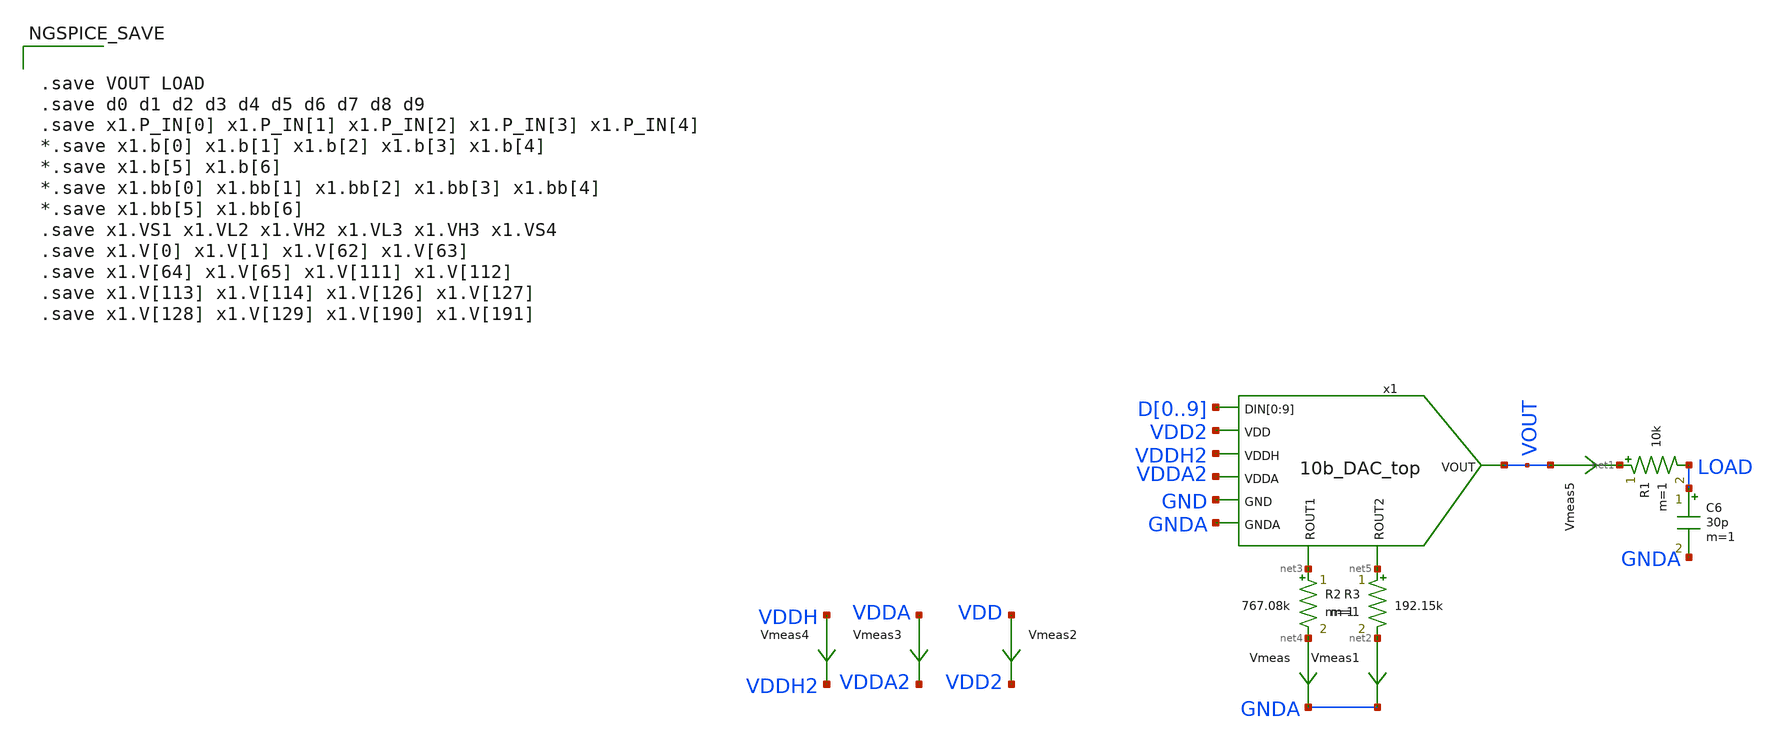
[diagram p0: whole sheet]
** sch_path: xschem/10b_DAC_noise-tb.sch
.lib $::SKYWATER_MODELS/sky130.lib.spice tt
.include $::SKYWATER_STDCELLS/sky130_fd_sc_hd.spice

**.subckt 10b_DAC_noise-tb
C6 LOAD GNDA 30p m=1
R1 net1 LOAD 10k m=1
Vmeas1 net2 GNDA 0
.save i(vmeas1)
R2 net3 net4 767.08k m=1
Vmeas net4 GNDA 0
.save i(vmeas)
R3 net5 net2 192.15k m=1
Vmeas2 VDD VDD2 0
.save i(vmeas2)
x1 D0 D1 D2 D3 D4 D5 D6 D7 D8 D9 VDD2 VDDH2 VDDA2 GND GNDA VOUT net3 net5 10b_DAC_top
Vmeas3 VDDA VDDA2 0
.save i(vmeas3)
Vmeas4 VDDH VDDH2 0
.save i(vmeas4)
Vmeas5 VOUT net1 0
.save i(vmeas5)
**** begin user architecture code


.save VOUT LOAD
.save d0 d1 d2 d3 d4 d5 d6 d7 d8 d9
.save x1.P_IN[0] x1.P_IN[1] x1.P_IN[2] x1.P_IN[3] x1.P_IN[4]
*.save x1.b[0] x1.b[1] x1.b[2] x1.b[3] x1.b[4]
*.save x1.b[5] x1.b[6]
*.save x1.bb[0] x1.bb[1] x1.bb[2] x1.bb[3] x1.bb[4]
*.save x1.bb[5] x1.bb[6]
.save x1.VS1 x1.VL2 x1.VH2 x1.VL3 x1.VH3 x1.VS4
.save x1.V[0] x1.V[1] x1.V[62] x1.V[63]
.save x1.V[64] x1.V[65] x1.V[111] x1.V[112]
.save x1.V[113] x1.V[114] x1.V[126] x1.V[127]
.save x1.V[128] x1.V[129] x1.V[190] x1.V[191]





  *.options wnflag=0 bypass=1
  .option wnflag=1
  .option safecurrents
  *.option klu
  .options solver=klu nomod
  .options method=gear rawfile=binary
  *.options reltol=1e-2 abstol=1e-12 chgtol=1e-14
  ********************Static Voltage Sources***************************
  Vddh vddh gnd dc 5.5
  Vdd vdd gnd dc 1.8
  Vdda vdda gnd dc 5.5
  Vgnda gnda gnd dc 0

  VHREF x1.V[191] GND 5.5
  VLREF x1.V[0] GND 0
  ********************Dynamic Voltage Sources***************************
  *******Calculation**********
  .param base_f=100e3 base_t={1/base_f} base_th={base_t/2} base_d={2*base_th}
  .param d0_th={base_th} d0_t={d0_th*2}
  .param d1_th={d0_th*2} d1_t={d1_th*2}
  .param d2_th={d1_th*2} d2_t={d2_th*2}
  .param d3_th={d2_th*2} d3_t={d3_th*2}
  .param d4_th={d3_th*2} d4_t={d4_th*2}
  .param d5_th={d4_th*2} d5_t={d5_th*2}
  .param d6_th={d5_th*2} d6_t={d6_th*2}
  .param d7_th={d6_th*2} d7_t={d7_th*2}
  .param d8_th={d7_th*2} d8_t={d8_th*2}
  .param d9_th={d8_th*2} d9_t={d9_th*2}

  .param delay_0 = {base_d}
  .param delay_1 = {delay_0 + d0_th}
  .param delay_2 = {delay_1}
  .param delay_3 = {delay_2 + d2_th}
  .param delay_4 = {delay_3 + d3_th}
  .param delay_5 = {delay_4 + d4_th}
  .param delay_6 = {delay_5 + d5_th}
  .param delay_7 = {delay_6}
  .param delay_8 = {delay_7 + d7_th}
  .param delay_9 = {delay_8}
  *******Signals**********
  .param vhi=1.8
  Vd0  d0  gnd pulse(0 {vhi} {delay_0} 1n 1n {d0_th} {d0_t})
  Vd1  d1  gnd pulse({vhi} 0 {delay_1} 1n 1n {d1_th} {d1_t})
  Vd2  d2  gnd pulse(0 {vhi} {delay_2} 1n 1n {d2_th} {d2_t})
  Vd3  d3  gnd pulse(0 {vhi} {delay_3} 1n 1n {d3_th} {d3_t})
  Vd4  d4  gnd pulse(0 {vhi} {delay_4} 1n 1n {d4_th} {d4_t})
  Vd5  d5  gnd pulse(0 {vhi} {delay_5} 1n 1n {d5_th} {d5_t})
  Vd6  d6  gnd pulse({vhi} 0 {delay_6} 1n 1n {d6_th} {d6_t})
  Vd7  d7  gnd pulse(0 {vhi} {delay_7} 1n 1n {d7_th} {d7_t})
  Vd8  d8  gnd pulse({vhi} 0 {delay_8} 1n 1n {d8_th} {d8_t})
  Vd9  d9  gnd pulse(0 {vhi} {delay_9} 1n 1n {d9_th} {d9_t})

  *Vd6  d6  gnd vhi
  *Vd7  d7  gnd 0
  *Vd8  d8  gnd vhi
  *Vd9  d9  gnd vhi
  ********************Simulation Commands*****************************
  .control
     reset
     set num_threads=36
     tran 1n 200u
     write 10b_DAC_tr3-tb.raw

     set wr_vecnames
     set wr_singlescale
     wrdata $THESIS_WS/simulations/top_tr3-tb.txt VOUT LOAD d0 d1 d2 d3 d4 d5 d6 d7 d8 d9

*    quit 0
  .endc



**** end user architecture code
**.ends
.end
